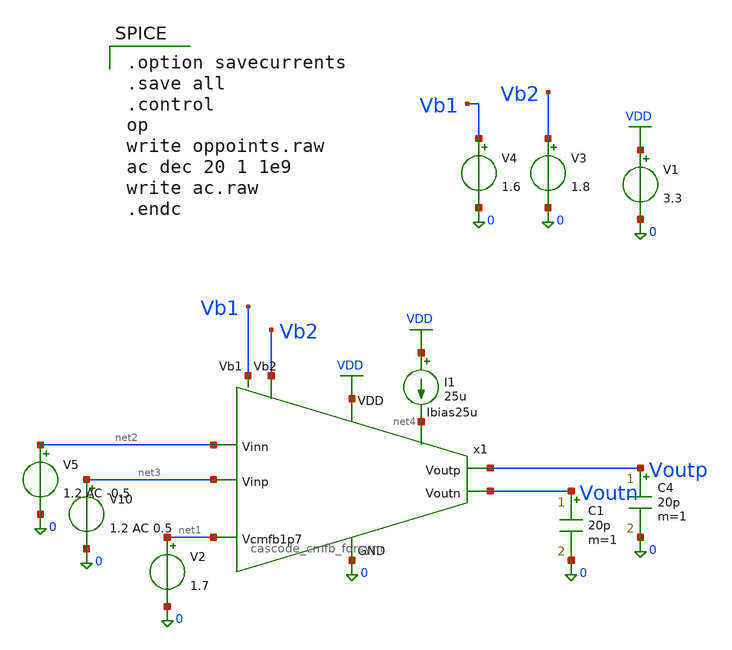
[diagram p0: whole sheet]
** sch_path: jz_fda/cascode_cmfb_forsym_tb.sch
**.subckt cascode_cmfb_forsym_tb
C4 Voutp 0 20p m=1
C1 Voutn 0 20p m=1
V1 VDD 0 3.3
V3 Vb2 0 1.8
V4 Vb1 0 1.6
I1 VDD net4 25u
V2 net1 0 1.7
V5 net2 0 1.2 AC -0.5
V10 net3 0 1.2 AC 0.5
x1 VDD Vb2 Voutp Voutn Vb1 net4 net2 net1 0 net3 cascode_cmfb_forsym
**** begin user architecture code

.option savecurrents
.save all
.control
op
write oppoints.raw
ac dec 20 1 1e9
write ac.raw
.endc


.include $::180MCU_MODELS/design.ngspice
.lib $::180MCU_MODELS/sm141064.ngspice typical
.lib $::180MCU_MODELS/smbb000149.ngspice typical

**** end user architecture code
**.ends
.GLOBAL VDD
.end
